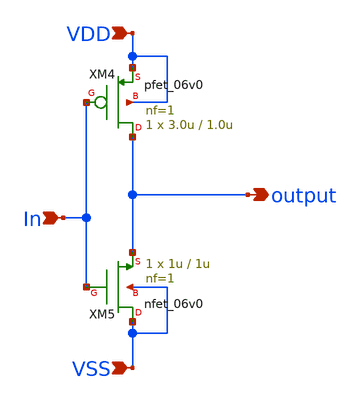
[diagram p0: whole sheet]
** sch_path: activities/opamp3AKAM/invertor.sch
**.subckt invertor output In VDD VSS
*.opin output
*.ipin In
*.ipin VDD
*.ipin VSS
XM4 output In VDD VDD pfet_06v0 L=1.0u W=3.0u nf=1 ad='int((nf+1)/2) * W/nf * 0.18u' as='int((nf+2)/2) * W/nf * 0.18u'
+ pd='2*int((nf+1)/2) * (W/nf + 0.18u)' ps='2*int((nf+2)/2) * (W/nf + 0.18u)' nrd='0.18u / W' nrs='0.18u / W'
+ sa=0 sb=0 sd=0 m=1
XM5 VSS In output VSS nfet_06v0 L=1u W=1u nf=1 ad='int((nf+1)/2) * W/nf * 0.18u' as='int((nf+2)/2) * W/nf * 0.18u'
+ pd='2*int((nf+1)/2) * (W/nf + 0.18u)' ps='2*int((nf+2)/2) * (W/nf + 0.18u)' nrd='0.18u / W' nrs='0.18u / W'
+ sa=0 sb=0 sd=0 m=1
**.ends
.end
